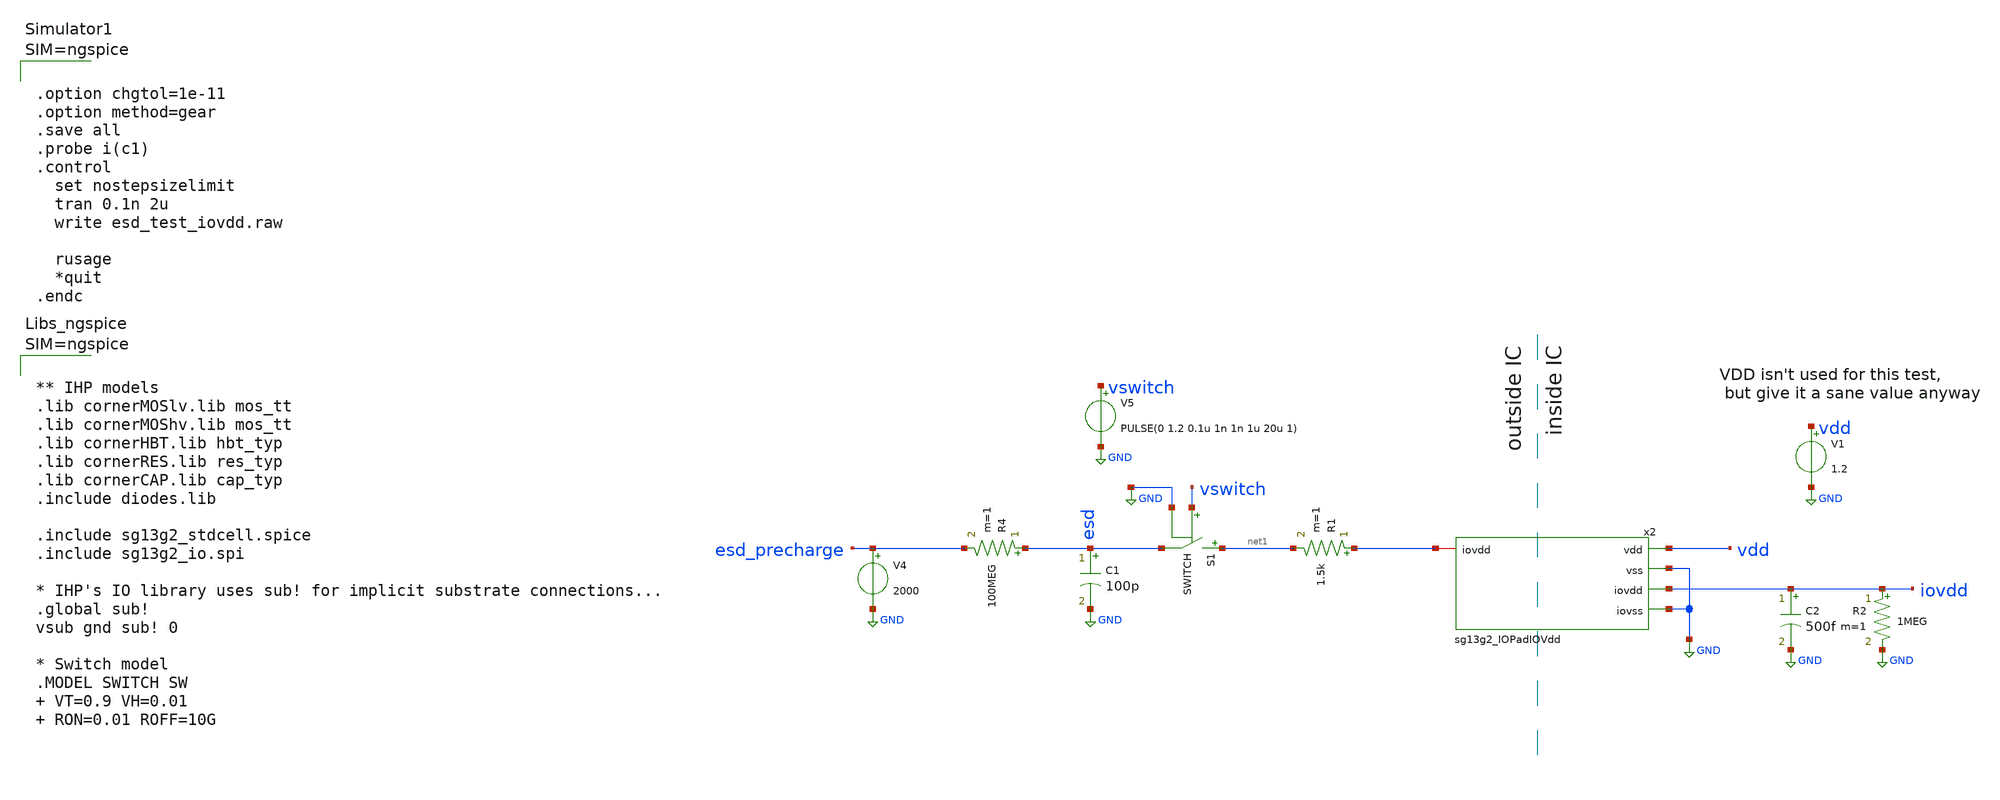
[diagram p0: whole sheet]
** sch_path: xschem/esd_test_iovdd.sch
**.subckt esd_test_iovdd
C1 esd GND 100p m=1
R1 iovdd net1 1.5k m=1
V1 vdd GND 1.2
S1 net1 esd vswitch GND SWITCH
x2 GND vdd GND iovdd sg13g2_IOPadIOVdd
V4 esd_precharge GND 2000
V5 vswitch GND PULSE(0 1.2 0.1u 1n 1n 1u 20u 1)
R4 esd esd_precharge 100MEG m=1
R2 iovdd GND 1MEG m=1
C2 iovdd GND 500f m=1
**** begin user architecture code



** IHP models
.lib cornerMOSlv.lib mos_tt
.lib cornerMOShv.lib mos_tt
.lib cornerHBT.lib hbt_typ
.lib cornerRES.lib res_typ
.lib cornerCAP.lib cap_typ
.include diodes.lib

.include sg13g2_stdcell.spice
.include sg13g2_io.spi

* IHP's IO library uses sub! for implicit substrate connections...
.global sub!
vsub gnd sub! 0

* Switch model
.MODEL SWITCH SW   VT=0.9 VH=0.01  RON=0.01 ROFF=10G





.option chgtol=1e-11
.option method=gear
.save all
.probe i(c1)
.control
  set nostepsizelimit
  tran 0.1n 2u
  write esd_test_iovdd.raw

  rusage
  *quit
.endc









**** end user architecture code
**.ends
.GLOBAL GND
.end
